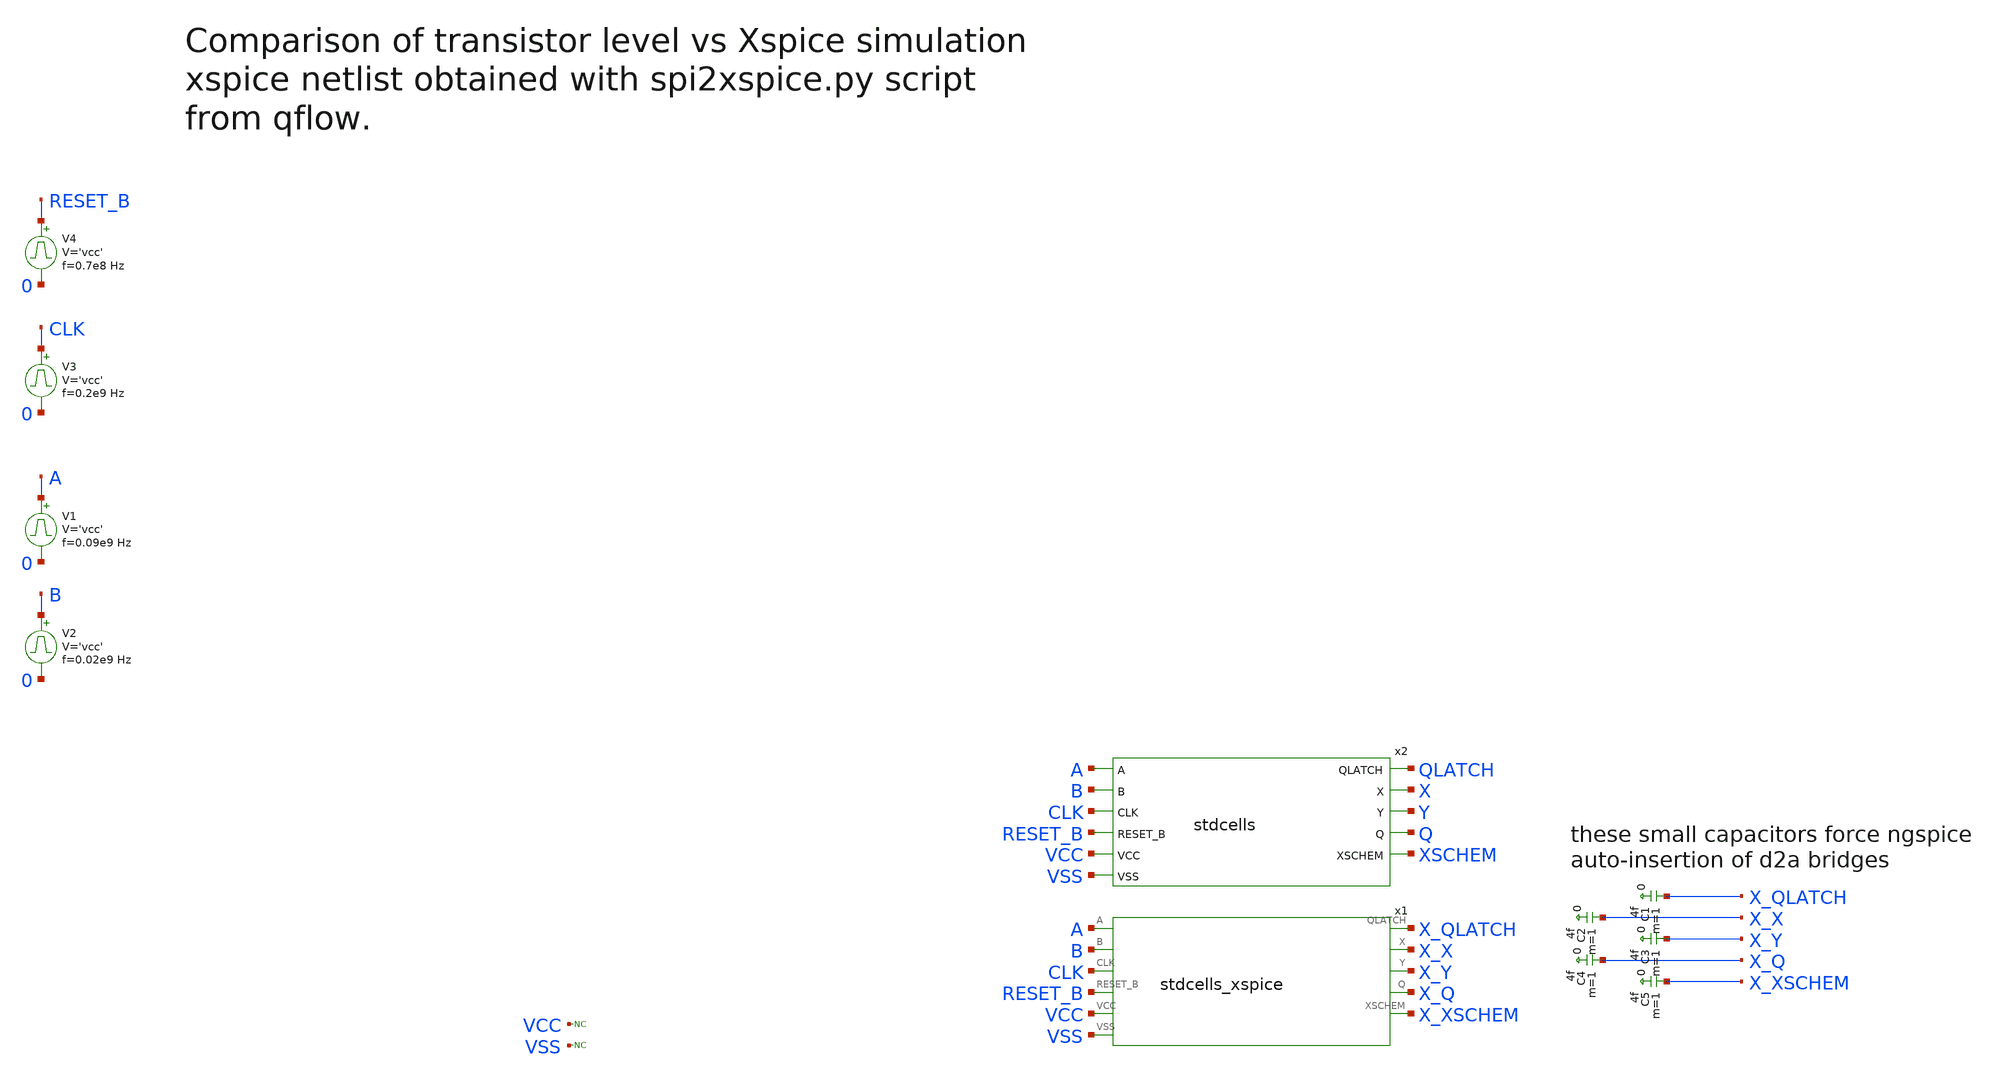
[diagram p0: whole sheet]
** sch_path: sky130A/xschem_libs/sky130_tests_ase/test_stdcells/schematic/test_stdcells.sch
* Copyright 2021 Stefan Frederik Schippers
* Licensed under the Apache License, Version 2.0 (the "License");
* you may not use this file except in compliance with the License.
* You may obtain a copy of the License at
* https://www.apache.org/licenses/LICENSE-2.0
* Unless required by applicable law or agreed to in writing, software
* distributed under the License is distributed on an "AS IS" BASIS,
* WITHOUT WARRANTIES OR CONDITIONS OF ANY KIND, either express or implied.
* See the License for the specific language governing permissions and
* limitations under the License.
**.subckt test_stdcells
V1 A 0 pulse 0 'vcc' '0.495/ 0.09e9 ' '0.01/0.09e9 ' '0.01/0.09e9 ' '0.49/0.09e9 ' '1/0.09e9 '
V2 B 0 pulse 0 'vcc' '0.495/ 0.02e9 ' '0.01/0.02e9 ' '0.01/0.02e9 ' '0.49/0.02e9 ' '1/0.02e9 '
V3 CLK 0 pulse 0 'vcc' '0.495/ 0.2e9 ' '0.01/0.2e9 ' '0.01/0.2e9 ' '0.49/0.2e9 ' '1/0.2e9 '
V4 RESET_B 0 pulse 0 'vcc' '0.495/ 0.7e8 ' '0.01/0.7e8 ' '0.01/0.7e8 ' '0.49/0.7e8 ' '1/0.7e8 '
x2 QLATCH A X B Y CLK Q RESET_B XSCHEM VCC VSS stdcells
x1 X_QLATCH A X_X B X_Y CLK X_Q RESET_B X_XSCHEM VCC VSS stdcells_xspice
* noconn VCC
* noconn VSS
C1 X_QLATCH 0 4f m=1
C2 X_X 0 4f m=1
C3 X_Y 0 4f m=1
C4 X_Q 0 4f m=1
C5 X_XSCHEM 0 4f m=1
**.ends
.end
